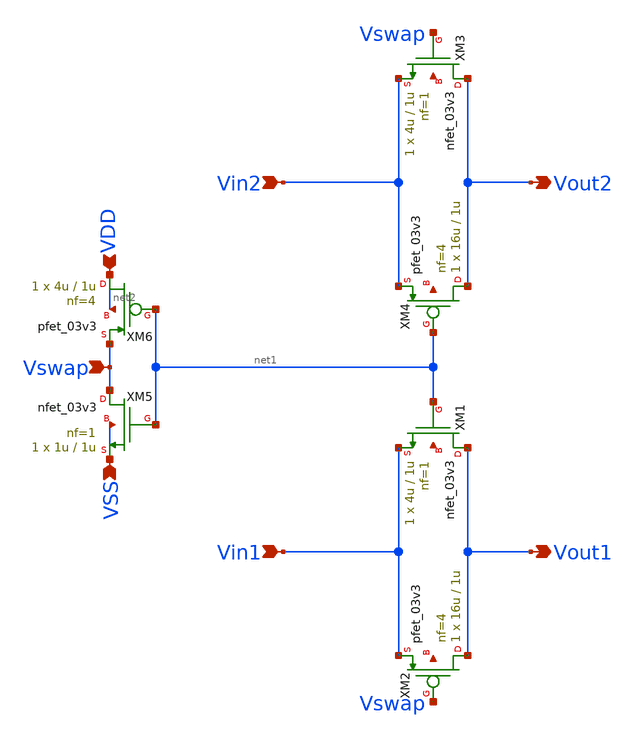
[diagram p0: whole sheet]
** sch_path: blocks/pll/mux.sch
**.subckt mux Vin1 Vout1 Vin2 Vout2 VDD VSS Vswap
*.ipin Vin1
*.opin Vout1
*.ipin Vin2
*.opin Vout2
*.ipin VDD
*.ipin VSS
*.ipin Vswap
XM1 Vout1 net1 Vin1 net3 nfet_03v3 L=1u W=4u nf=1 ad='int((nf+1)/2) * W/nf * 0.18u' as='int((nf+2)/2) * W/nf * 0.18u'
+ pd='2*int((nf+1)/2) * (W/nf + 0.18u)' ps='2*int((nf+2)/2) * (W/nf + 0.18u)' nrd='0.18u / W' nrs='0.18u / W'
+ sa=0 sb=0 sd=0 m=1
XM2 Vout1 Vswap Vin1 net4 pfet_03v3 L=1u W=16u nf=4 ad='int((nf+1)/2) * W/nf * 0.18u' as='int((nf+2)/2) * W/nf * 0.18u'
+ pd='2*int((nf+1)/2) * (W/nf + 0.18u)' ps='2*int((nf+2)/2) * (W/nf + 0.18u)' nrd='0.18u / W' nrs='0.18u / W'
+ sa=0 sb=0 sd=0 m=1
XM3 Vout2 Vswap Vin2 net5 nfet_03v3 L=1u W=4u nf=1 ad='int((nf+1)/2) * W/nf * 0.18u' as='int((nf+2)/2) * W/nf * 0.18u'
+ pd='2*int((nf+1)/2) * (W/nf + 0.18u)' ps='2*int((nf+2)/2) * (W/nf + 0.18u)' nrd='0.18u / W' nrs='0.18u / W'
+ sa=0 sb=0 sd=0 m=1
XM4 Vout2 net1 Vin2 net6 pfet_03v3 L=1u W=16u nf=4 ad='int((nf+1)/2) * W/nf * 0.18u' as='int((nf+2)/2) * W/nf * 0.18u'
+ pd='2*int((nf+1)/2) * (W/nf + 0.18u)' ps='2*int((nf+2)/2) * (W/nf + 0.18u)' nrd='0.18u / W' nrs='0.18u / W'
+ sa=0 sb=0 sd=0 m=1
XM5 Vswap net1 VSS VSS nfet_03v3 L=1u W=1u nf=1 ad='int((nf+1)/2) * W/nf * 0.18u' as='int((nf+2)/2) * W/nf * 0.18u'
+ pd='2*int((nf+1)/2) * (W/nf + 0.18u)' ps='2*int((nf+2)/2) * (W/nf + 0.18u)' nrd='0.18u / W' nrs='0.18u / W'
+ sa=0 sb=0 sd=0 m=1
XM6 VDD net1 Vswap net2 pfet_03v3 L=1u W=4u nf=4 ad='int((nf+1)/2) * W/nf * 0.18u' as='int((nf+2)/2) * W/nf * 0.18u'
+ pd='2*int((nf+1)/2) * (W/nf + 0.18u)' ps='2*int((nf+2)/2) * (W/nf + 0.18u)' nrd='0.18u / W' nrs='0.18u / W'
+ sa=0 sb=0 sd=0 m=1
**.ends
.end
